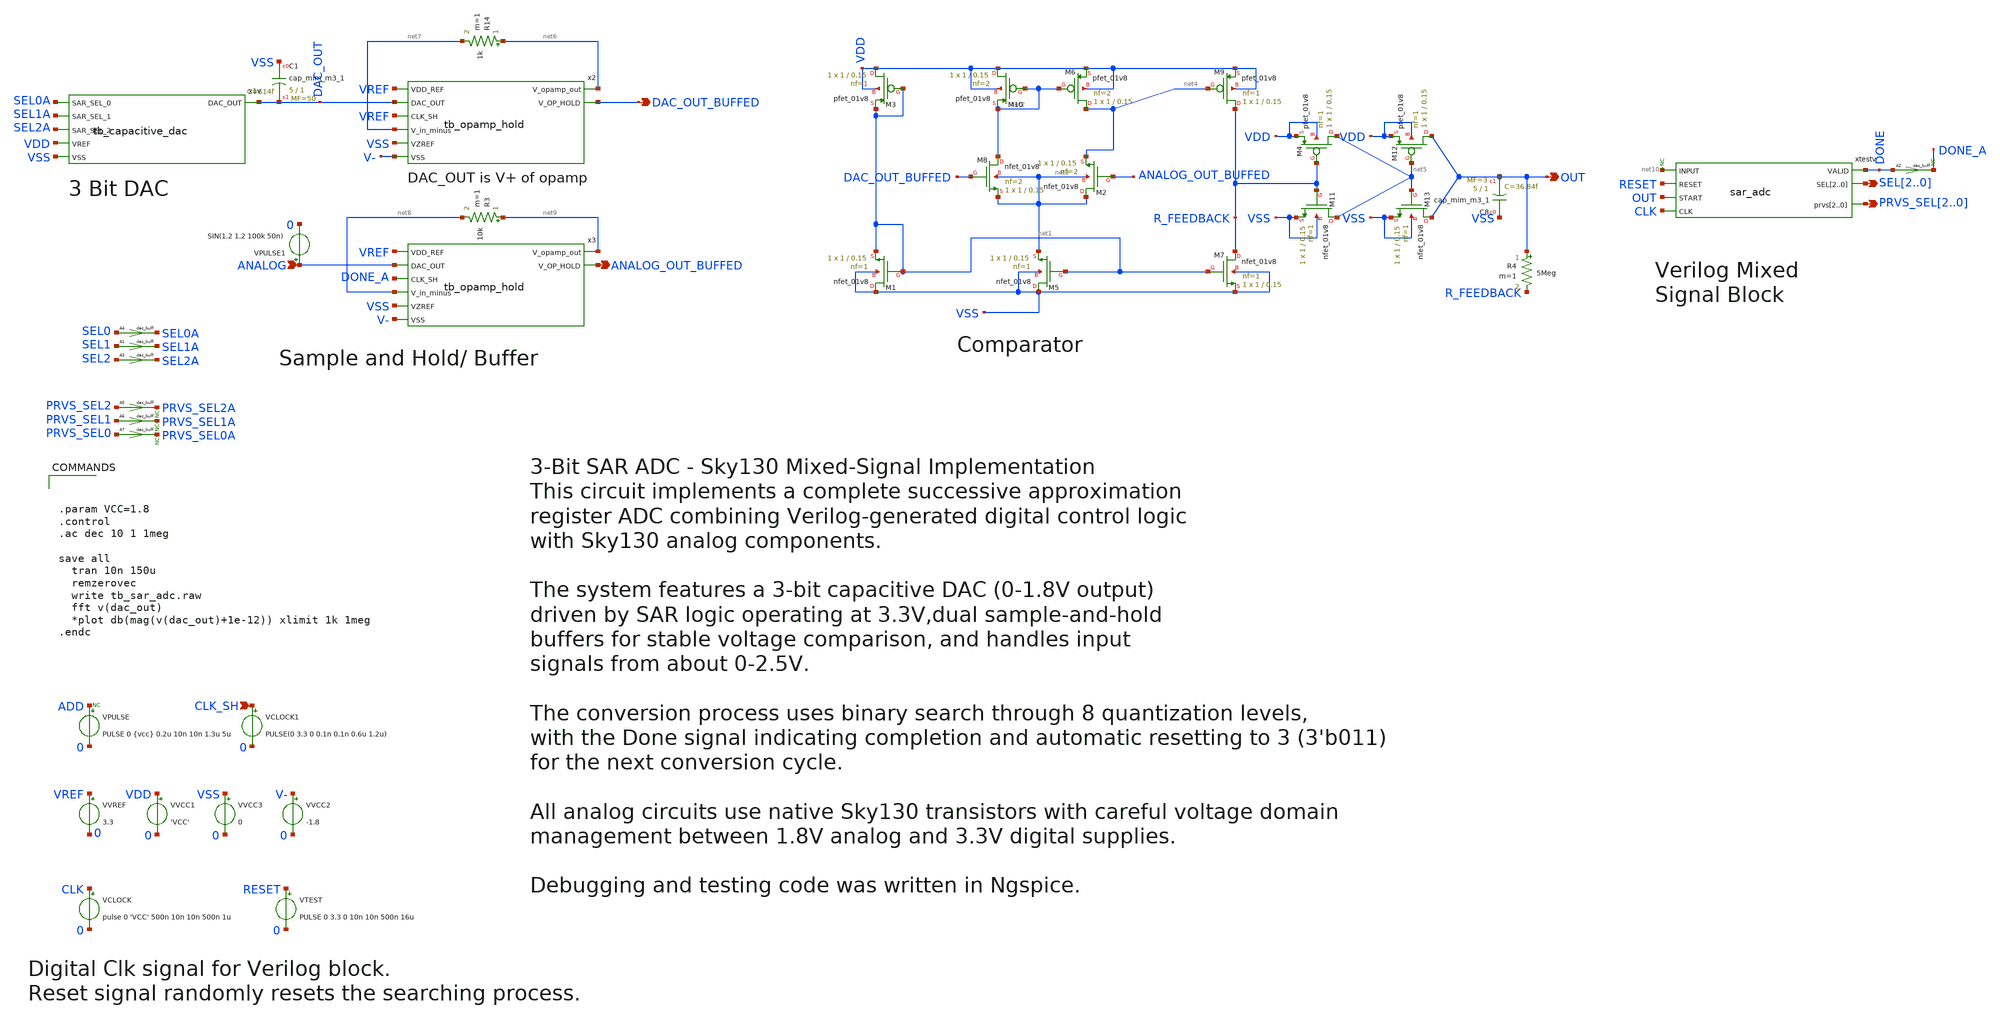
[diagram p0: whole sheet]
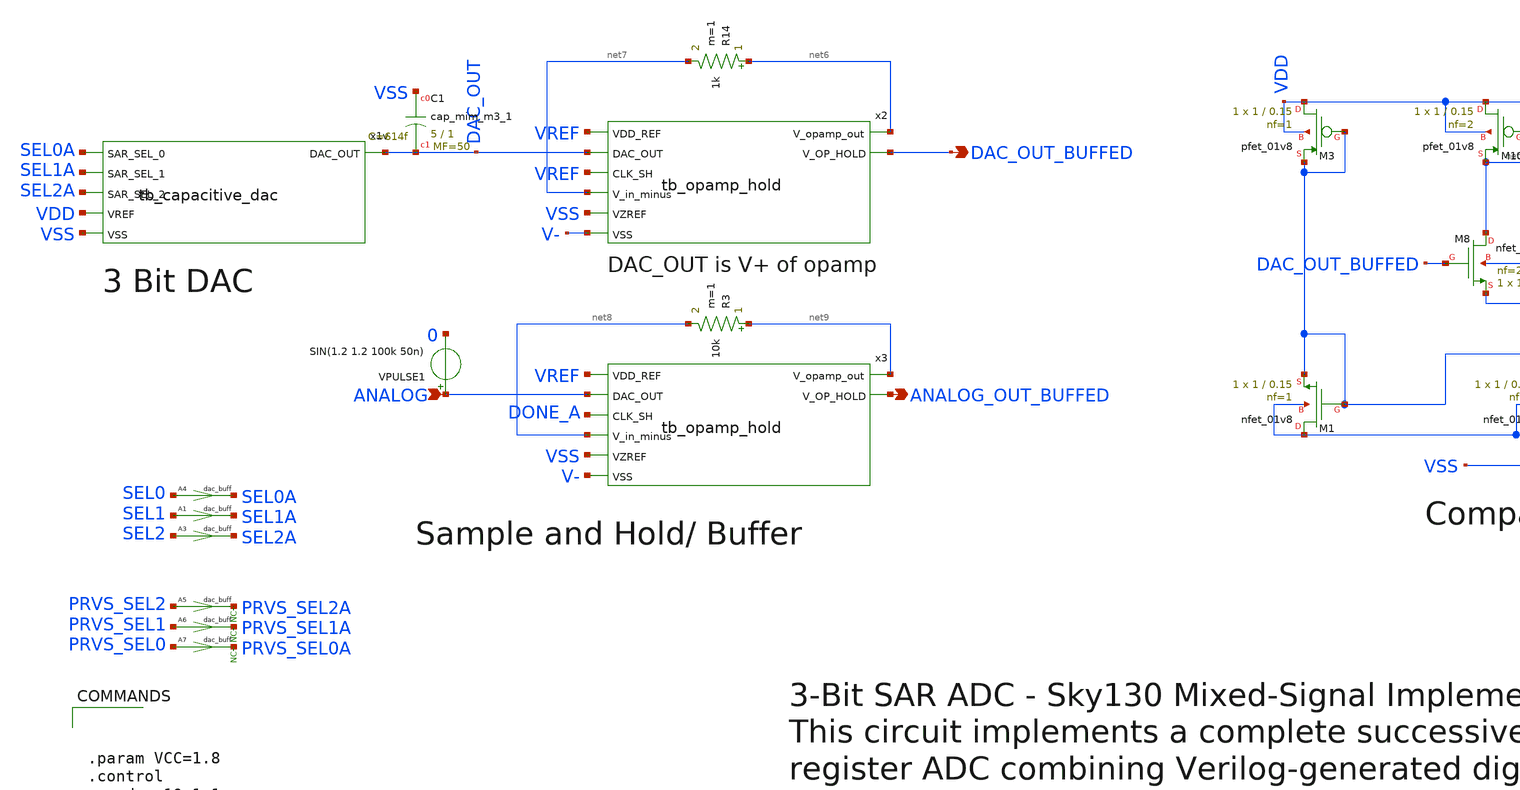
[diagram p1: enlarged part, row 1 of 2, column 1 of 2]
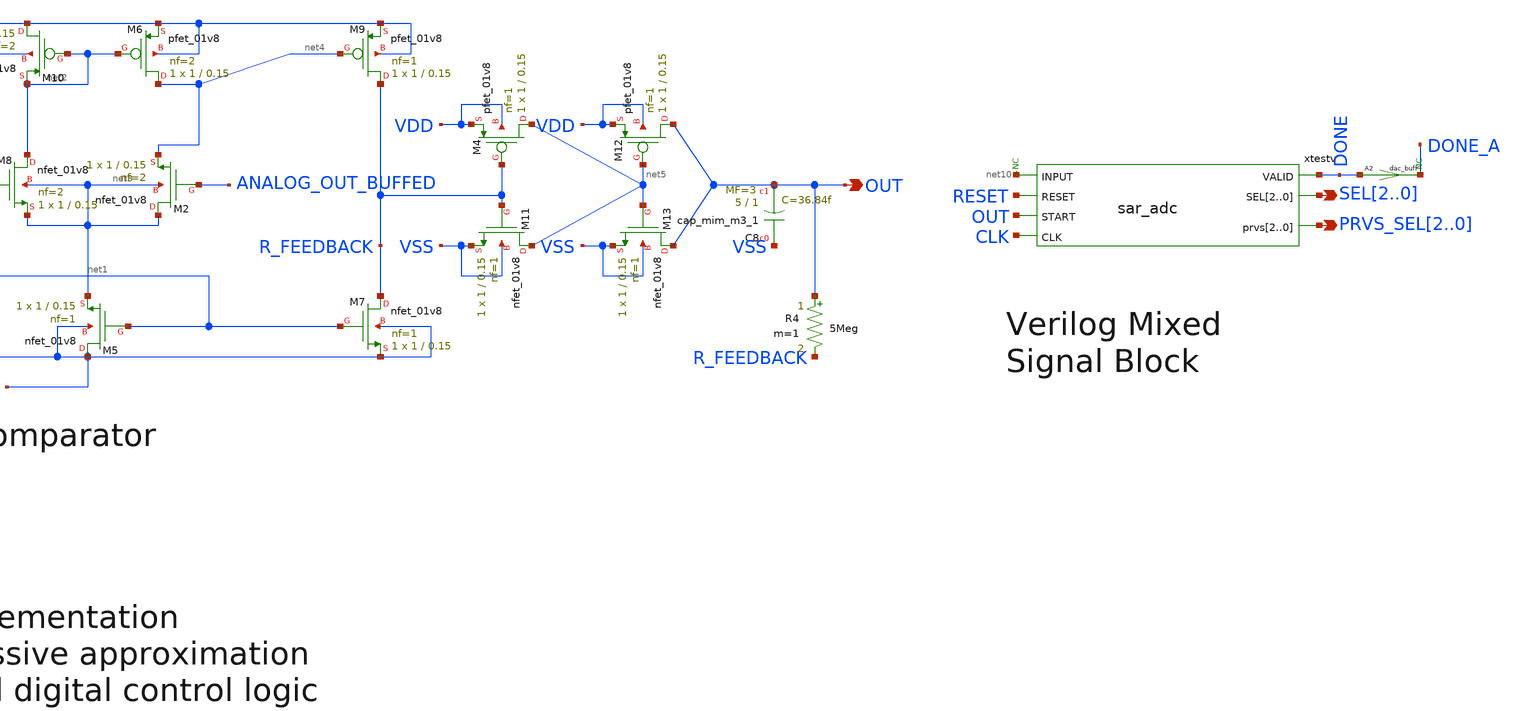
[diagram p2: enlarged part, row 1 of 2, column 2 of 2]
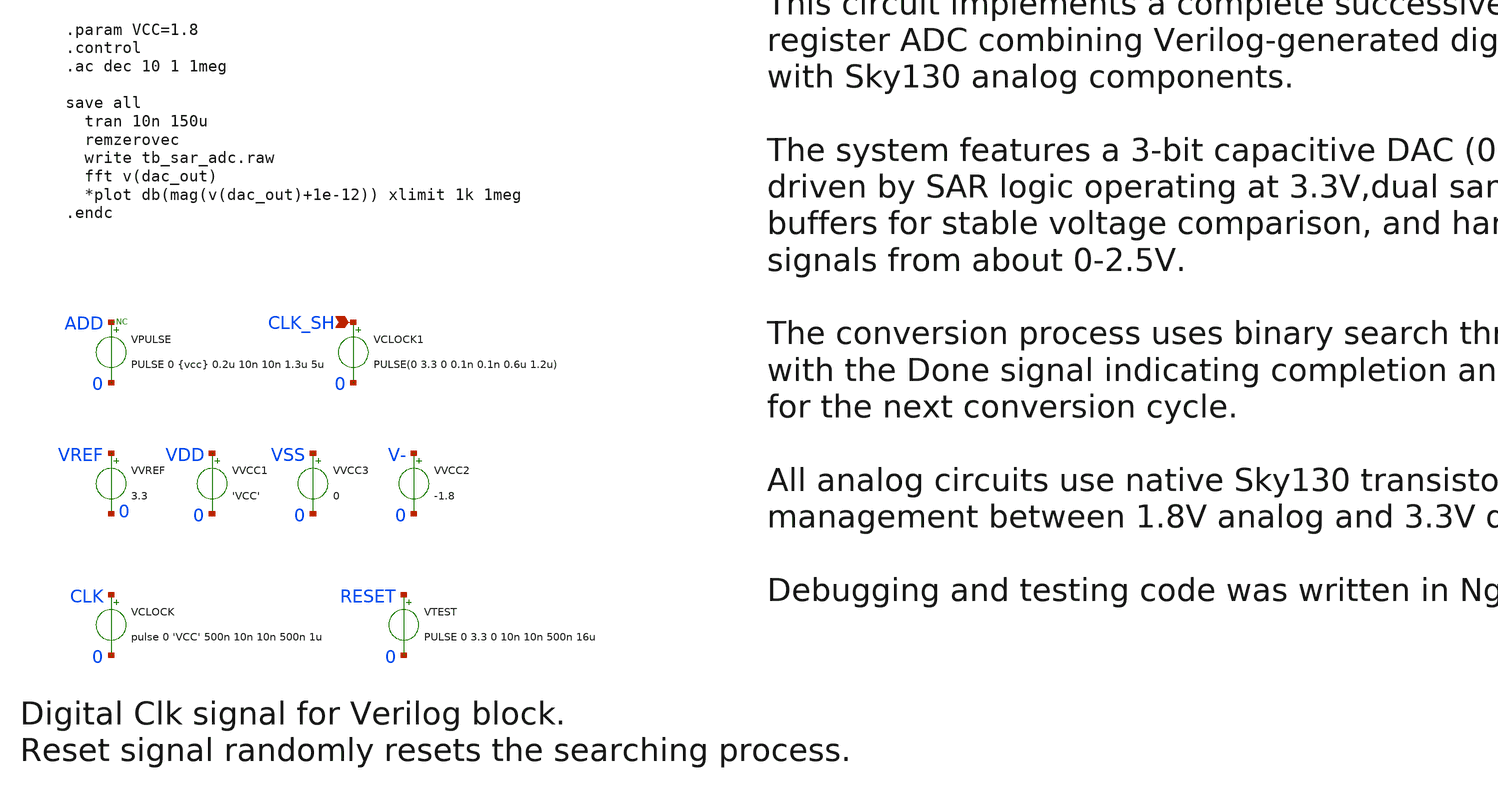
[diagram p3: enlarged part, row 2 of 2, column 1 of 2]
** sch_path: 3bit_sar_adc/tb_sar_adc.sch
**.subckt tb_sar_adc SEL2,SEL1,SEL0 PRVS_SEL2,PRVS_SEL1,PRVS_SEL0 OUT ANALOG DAC_OUT_BUFFED
*+ ANALOG_OUT_BUFFED CLK_SH
*.opin SEL2,SEL1,SEL0
*.opin PRVS_SEL2,PRVS_SEL1,PRVS_SEL0
*.opin OUT
*.ipin ANALOG
*.opin DAC_OUT_BUFFED
*.opin ANALOG_OUT_BUFFED
*.ipin CLK_SH
VPULSE ADD 0 PULSE 0 {vcc} 0.2u 10n 10n 1.3u 5u
VTEST RESET 0 PULSE 0 3.3 0 10n 10n 500n 16u
xtestv net10 RESET OUT DONE SEL2 SEL1 SEL0 CLK PRVS_SEL2 PRVS_SEL1 PRVS_SEL0 sar_adc
A2 [ DONE ] [ DONE_A ] dac_buff
VCLOCK CLK 0 pulse 0 'VCC' 500n 10n 10n 500n 1u
A1 [ SEL1 ] [ SEL1A ] dac_buff
A3 [ SEL2 ] [ SEL2A ] dac_buff
A4 [ SEL0 ] [ SEL0A ] dac_buff
A5 [ PRVS_SEL2 ] [ PRVS_SEL2A ] dac_buff
A6 [ PRVS_SEL1 ] [ PRVS_SEL1A ] dac_buff
A7 [ PRVS_SEL0 ] [ PRVS_SEL0A ] dac_buff
XM9 R_FEEDBACK net4 VDD VDD sky130_fd_pr__pfet_01v8 L=0.15 W=1 nf=1 ad='int((nf+1)/2) * W/nf * 0.29'
+ as='int((nf+2)/2) * W/nf * 0.29' pd='2*int((nf+1)/2) * (W/nf + 0.29)' ps='2*int((nf+2)/2) * (W/nf + 0.29)'
+ nrd='0.29 / W' nrs='0.29 / W' sa=0 sb=0 sd=0 mult=1 m=1
XM6 net4 net2 VDD VDD sky130_fd_pr__pfet_01v8 L=0.15 W=1 nf=2 ad='int((nf+1)/2) * W/nf * 0.29' as='int((nf+2)/2) * W/nf * 0.29'
+ pd='2*int((nf+1)/2) * (W/nf + 0.29)' ps='2*int((nf+2)/2) * (W/nf + 0.29)' nrd='0.29 / W' nrs='0.29 / W'
+ sa=0 sb=0 sd=0 mult=1 m=1
XM10 VDD net2 net2 VDD sky130_fd_pr__pfet_01v8 L=0.15 W=1 nf=2 ad='int((nf+1)/2) * W/nf * 0.29' as='int((nf+2)/2) * W/nf * 0.29'
+ pd='2*int((nf+1)/2) * (W/nf + 0.29)' ps='2*int((nf+2)/2) * (W/nf + 0.29)' nrd='0.29 / W' nrs='0.29 / W'
+ sa=0 sb=0 sd=0 mult=1 m=1
XM3 VDD net1 net1 VDD sky130_fd_pr__pfet_01v8 L=0.15 W=1 nf=1 ad='int((nf+1)/2) * W/nf * 0.29' as='int((nf+2)/2) * W/nf * 0.29'
+ pd='2*int((nf+1)/2) * (W/nf + 0.29)' ps='2*int((nf+2)/2) * (W/nf + 0.29)' nrd='0.29 / W' nrs='0.29 / W'
+ sa=0 sb=0 sd=0 mult=1 m=1
XM4 net5 R_FEEDBACK VDD VDD sky130_fd_pr__pfet_01v8 L=0.15 W=1 nf=1 ad='int((nf+1)/2) * W/nf * 0.29'
+ as='int((nf+2)/2) * W/nf * 0.29' pd='2*int((nf+1)/2) * (W/nf + 0.29)' ps='2*int((nf+2)/2) * (W/nf + 0.29)'
+ nrd='0.29 / W' nrs='0.29 / W' sa=0 sb=0 sd=0 mult=1 m=1
XM12 OUT net5 VDD VDD sky130_fd_pr__pfet_01v8 L=0.15 W=1 nf=1 ad='int((nf+1)/2) * W/nf * 0.29' as='int((nf+2)/2) * W/nf * 0.29'
+ pd='2*int((nf+1)/2) * (W/nf + 0.29)' ps='2*int((nf+2)/2) * (W/nf + 0.29)' nrd='0.29 / W' nrs='0.29 / W'
+ sa=0 sb=0 sd=0 mult=1 m=1
XM2 net3 ANALOG_OUT_BUFFED net4 net3 sky130_fd_pr__nfet_01v8 L=0.15 W=1 nf=2 ad='int((nf+1)/2) * W/nf * 0.29'
+ as='int((nf+2)/2) * W/nf * 0.29' pd='2*int((nf+1)/2) * (W/nf + 0.29)' ps='2*int((nf+2)/2) * (W/nf + 0.29)'
+ nrd='0.29 / W' nrs='0.29 / W' sa=0 sb=0 sd=0 mult=1 m=1
XM1 VSS net1 net1 VSS sky130_fd_pr__nfet_01v8 L=0.15 W=1 nf=1 ad='int((nf+1)/2) * W/nf * 0.29' as='int((nf+2)/2) * W/nf * 0.29'
+ pd='2*int((nf+1)/2) * (W/nf + 0.29)' ps='2*int((nf+2)/2) * (W/nf + 0.29)' nrd='0.29 / W' nrs='0.29 / W'
+ sa=0 sb=0 sd=0 mult=1 m=1
XM5 VSS net1 net3 VSS sky130_fd_pr__nfet_01v8 L=0.15 W=1 nf=1 ad='int((nf+1)/2) * W/nf * 0.29' as='int((nf+2)/2) * W/nf * 0.29'
+ pd='2*int((nf+1)/2) * (W/nf + 0.29)' ps='2*int((nf+2)/2) * (W/nf + 0.29)' nrd='0.29 / W' nrs='0.29 / W'
+ sa=0 sb=0 sd=0 mult=1 m=1
XM7 R_FEEDBACK net1 VSS VSS sky130_fd_pr__nfet_01v8 L=0.15 W=1 nf=1 ad='int((nf+1)/2) * W/nf * 0.29'
+ as='int((nf+2)/2) * W/nf * 0.29' pd='2*int((nf+1)/2) * (W/nf + 0.29)' ps='2*int((nf+2)/2) * (W/nf + 0.29)'
+ nrd='0.29 / W' nrs='0.29 / W' sa=0 sb=0 sd=0 mult=1 m=1
XM8 net2 DAC_OUT_BUFFED net3 net3 sky130_fd_pr__nfet_01v8 L=0.15 W=1 nf=2 ad='int((nf+1)/2) * W/nf * 0.29'
+ as='int((nf+2)/2) * W/nf * 0.29' pd='2*int((nf+1)/2) * (W/nf + 0.29)' ps='2*int((nf+2)/2) * (W/nf + 0.29)'
+ nrd='0.29 / W' nrs='0.29 / W' sa=0 sb=0 sd=0 mult=1 m=1
XM11 net5 R_FEEDBACK VSS VSS sky130_fd_pr__nfet_01v8 L=0.15 W=1 nf=1 ad='int((nf+1)/2) * W/nf * 0.29'
+ as='int((nf+2)/2) * W/nf * 0.29' pd='2*int((nf+1)/2) * (W/nf + 0.29)' ps='2*int((nf+2)/2) * (W/nf + 0.29)'
+ nrd='0.29 / W' nrs='0.29 / W' sa=0 sb=0 sd=0 mult=1 m=1
XM13 OUT net5 VSS VSS sky130_fd_pr__nfet_01v8 L=0.15 W=1 nf=1 ad='int((nf+1)/2) * W/nf * 0.29' as='int((nf+2)/2) * W/nf * 0.29'
+ pd='2*int((nf+1)/2) * (W/nf + 0.29)' ps='2*int((nf+2)/2) * (W/nf + 0.29)' nrd='0.29 / W' nrs='0.29 / W'
+ sa=0 sb=0 sd=0 mult=1 m=1
XC8 VSS OUT sky130_fd_pr__cap_mim_m3_1 W=5 L=1 MF=3 m=3
VVCC1 VDD 0 'VCC'
VPULSE1 ANALOG 0 SIN(1.2 1.2 100k 50n)
x1v DAC_OUT SEL0A SEL1A SEL2A VDD VSS tb_capacitive_dac
x2 VREF DAC_OUT VREF net7 net6 DAC_OUT_BUFFED VSS V- tb_opamp_hold
VVREF VREF 0 3.3
x3 VREF ANALOG DONE_A net8 net9 ANALOG_OUT_BUFFED VSS V- tb_opamp_hold
VVCC3 VSS 0 0
VVCC2 V- 0 -1.8
* noconn DONE_A
* noconn ADD
* noconn PRVS_SEL2A
* noconn PRVS_SEL1A
* noconn PRVS_SEL0A
VCLOCK1 CLK_SH 0 PULSE(0 3.3 0 0.1n 0.1n 0.6u 1.2u)
* noconn #net10
XC1 VSS DAC_OUT sky130_fd_pr__cap_mim_m3_1 W=5 L=1 MF=50 m=50
R14 net6 net7 1k m=1
R3 net9 net8 10k m=1
R4 OUT R_FEEDBACK 5Meg m=1
**** begin user architecture code



.param VCC=1.8
.control
.ac dec 10 1 1meg

save all
  tran 10n 150u
  remzerovec
  write tb_sar_adc.raw
  fft v(dac_out)
  *plot db(mag(v(dac_out)+1e-12)) xlimit 1k 1meg
.endc



** opencircuitdesign pdks install
.lib $::SKYWATER_MODELS/sky130.lib.spice tt
.include $::SKYWATER_STDCELLS/sky130_fd_sc_hd.spice
.include /foss/pdks/sky130A/libs.tech/xschem/sky130_stdcells/

**** end user architecture code
**.ends

* expanding   symbol:  /headless/Documents/3bit_sar_adc/sar_adc.sym # of pins=7
** sym_path: 3bit_sar_adc/sar_adc.sym
** sch_path: 3bit_sar_adc/sar_adc.sch
.subckt sar_adc INPUT RESET START VALID SEL2 SEL1 SEL0 CLK prvs2 prvs1 prvs0
*.ipin INPUT
*.ipin RESET
*.ipin START
*.opin VALID
*.ipin CLK
*.opin SEL2,SEL1,SEL0
*.opin prvs2,prvs1,prvs0
ACOMP [ net2 ] [ net1 ] comparator
ADUT [ CLK RESET START ] [ VALID SEL2 SEL1 SEL0 prvs2 prvs1 prvs0 ] dut
A1 [ COMP ] [ COMP_A ] dac_buff
* noconn #net1
* noconn #net2
* noconn COMP_A
* noconn COMP
* noconn INPUT
.ends


* expanding   symbol:  /headless/Documents/3bit_sar_adc/tb_capacitive_dac.sym # of pins=6
** sym_path: 3bit_sar_adc/tb_capacitive_dac.sym
** sch_path: 3bit_sar_adc/tb_capacitive_dac.sch
.subckt tb_capacitive_dac DAC_OUT SAR_SEL_0 SAR_SEL_1 SAR_SEL_2 VREF VSS
*.opin DAC_OUT
*.ipin SAR_SEL_1
*.ipin SAR_SEL_0
*.ipin SAR_SEL_2
*.ipin VREF
*.ipin VSS
XM20 VSS SAR_SEL_2 S2 S2 sky130_fd_pr__pfet_01v8 L=0.15 W=100 nf=4 ad='int((nf+1)/2) * W/nf * 0.29' as='int((nf+2)/2) * W/nf * 0.29'
+ pd='2*int((nf+1)/2) * (W/nf + 0.29)' ps='2*int((nf+2)/2) * (W/nf + 0.29)' nrd='0.29 / W' nrs='0.29 / W'
+ sa=0 sb=0 sd=0 mult=1 m=1
XM21 VREF SAR_SEL_2 S2 S2 sky130_fd_pr__nfet_01v8 L=0.15 W=150 nf=4 ad='int((nf+1)/2) * W/nf * 0.29'
+ as='int((nf+2)/2) * W/nf * 0.29' pd='2*int((nf+1)/2) * (W/nf + 0.29)' ps='2*int((nf+2)/2) * (W/nf + 0.29)'
+ nrd='0.29 / W' nrs='0.29 / W' sa=0 sb=0 sd=0 mult=1 m=1
XC16 net1 S1 sky130_fd_pr__cap_mim_m3_1 W=5 L=1 MF=400 m=400
XC18 net1 S0 sky130_fd_pr__cap_mim_m3_1 W=5 L=1 MF=200 m=200
XM22 VSS SAR_SEL_1 S1 S1 sky130_fd_pr__pfet_01v8 L=0.15 W=100 nf=10 ad='int((nf+1)/2) * W/nf * 0.29'
+ as='int((nf+2)/2) * W/nf * 0.29' pd='2*int((nf+1)/2) * (W/nf + 0.29)' ps='2*int((nf+2)/2) * (W/nf + 0.29)'
+ nrd='0.29 / W' nrs='0.29 / W' sa=0 sb=0 sd=0 mult=1 m=1
XM23 VREF SAR_SEL_1 S1 S1 sky130_fd_pr__nfet_01v8 L=0.15 W=150 nf=4 ad='int((nf+1)/2) * W/nf * 0.29'
+ as='int((nf+2)/2) * W/nf * 0.29' pd='2*int((nf+1)/2) * (W/nf + 0.29)' ps='2*int((nf+2)/2) * (W/nf + 0.29)'
+ nrd='0.29 / W' nrs='0.29 / W' sa=0 sb=0 sd=0 mult=1 m=1
XM24 VSS SAR_SEL_0 S0 S0 sky130_fd_pr__pfet_01v8 L=0.15 W=100 nf=4 ad='int((nf+1)/2) * W/nf * 0.29' as='int((nf+2)/2) * W/nf * 0.29'
+ pd='2*int((nf+1)/2) * (W/nf + 0.29)' ps='2*int((nf+2)/2) * (W/nf + 0.29)' nrd='0.29 / W' nrs='0.29 / W'
+ sa=0 sb=0 sd=0 mult=1 m=1
XM25 VREF SAR_SEL_0 S0 S0 sky130_fd_pr__nfet_01v8 L=0.15 W=150 nf=4 ad='int((nf+1)/2) * W/nf * 0.29'
+ as='int((nf+2)/2) * W/nf * 0.29' pd='2*int((nf+1)/2) * (W/nf + 0.29)' ps='2*int((nf+2)/2) * (W/nf + 0.29)'
+ nrd='0.29 / W' nrs='0.29 / W' sa=0 sb=0 sd=0 mult=1 m=1
XC22 DAC_OUT VSS sky130_fd_pr__cap_mim_m3_1 W=5 L=1 MF=20 m=20
XC2 net1 S2 sky130_fd_pr__cap_mim_m3_1 W=5 L=1 MF=825 m=825
XC6 VSS S2 sky130_fd_pr__cap_mim_m3_1 W=5 L=1 MF=200 m=200
XC5 VSS S1 sky130_fd_pr__cap_mim_m3_1 W=5 L=1 MF=200 m=200
XC7 VSS S0 sky130_fd_pr__cap_mim_m3_1 W=5 L=1 MF=100 m=100
**** begin user architecture code




.param CAP=80



**** end user architecture code
R1 net1 DAC_OUT 10 m=1
.ends


* expanding   symbol:  /headless/Documents/3bit_sar_adc/tb_opamp_hold.sym # of pins=8
** sym_path: 3bit_sar_adc/tb_opamp_hold.sym
** sch_path: 3bit_sar_adc/tb_opamp_hold.sch
.subckt tb_opamp_hold VDD_REF DAC_OUT CLK_SH V_in_minus V_opamp_out V_OP_HOLD VZREF VSS
*.opin V_opamp_out
*.ipin DAC_OUT
*.ipin CLK_SH
*.opin V_OP_HOLD
*.ipin VDD_REF
*.ipin VZREF
*.ipin VSS
*.ipin V_in_minus
XM82 net1 V_in_minus net3 net3 sky130_fd_pr__pfet_01v8 L=0.6 W=6 nf=1 ad='W * 0.29' as='W * 0.29' pd='2 * (W + 0.29)'
+ ps='2 * (W + 0.29)' nrd='0.29 / W' nrs='0.29 / W' sa=0 sb=0 sd=0 mult=1 m=1
XM84 net2 DAC_OUT net3 net3 sky130_fd_pr__pfet_01v8 L=0.6 W=6 nf=1 ad='W * 0.29' as='W * 0.29' pd='2 * (W + 0.29)'
+ ps='2 * (W + 0.29)' nrd='0.29 / W' nrs='0.29 / W' sa=0 sb=0 sd=0 mult=1 m=1
XM85 net1 net1 VSS VSS sky130_fd_pr__nfet_01v8 L=0.6 W=6 nf=1 ad='W * 0.29' as='W * 0.29' pd='2 * (W + 0.29)'
+ ps='2 * (W + 0.29)' nrd='0.29 / W' nrs='0.29 / W' sa=0 sb=0 sd=0 mult=1 m=1
XM86 net2 net1 VSS VSS sky130_fd_pr__nfet_01v8 L=0.6 W=6 nf=1 ad='W * 0.29' as='W * 0.29' pd='2 * (W + 0.29)'
+ ps='2 * (W + 0.29)' nrd='0.29 / W' nrs='0.29 / W' sa=0 sb=0 sd=0 mult=1 m=1
XM87 net3 VSS VDD_REF VDD_REF sky130_fd_pr__pfet_01v8 L=0.6 W=6 nf=1 ad='W * 0.29' as='W * 0.29' pd='2 * (W + 0.29)'
+ ps='2 * (W + 0.29)' nrd='0.29 / W' nrs='0.29 / W' sa=0 sb=0 sd=0 mult=1 m=1
XM88 V_opamp_out VSS VDD_REF VDD_REF sky130_fd_pr__pfet_01v8 L=0.6 W=6 nf=1 ad='W * 0.29' as='W * 0.29'
+ pd='2 * (W + 0.29)' ps='2 * (W + 0.29)' nrd='0.29 / W' nrs='0.29 / W' sa=0 sb=0 sd=0 mult=1 m=1
XM89 VZREF VSS VDD_REF VDD_REF sky130_fd_pr__pfet_01v8 L=0.6 W=6 nf=1 ad='W * 0.29' as='W * 0.29' pd='2 * (W + 0.29)'
+ ps='2 * (W + 0.29)' nrd='0.29 / W' nrs='0.29 / W' sa=0 sb=0 sd=0 mult=1 m=1
XM90 net4 VDD_REF net2 VSS sky130_fd_pr__nfet_01v8 L=0.6 W=1 nf=1 ad='W * 0.29' as='W * 0.29' pd='2 * (W + 0.29)'
+ ps='2 * (W + 0.29)' nrd='0.29 / W' nrs='0.29 / W' sa=0 sb=0 sd=0 mult=1 m=1
XM91 V_opamp_out net2 VSS VSS sky130_fd_pr__nfet_01v8 L=0.6 W=6 nf=1 ad='W * 0.29' as='W * 0.29' pd='2 * (W + 0.29)'
+ ps='2 * (W + 0.29)' nrd='0.29 / W' nrs='0.29 / W' sa=0 sb=0 sd=0 mult=1 m=1
XR10 VSS VZREF VSS sky130_fd_pr__res_high_po W=1 L=1 mult=1 m=1
XR13 VZREF VDD_REF VSS sky130_fd_pr__res_high_po W=1 L=1 mult=1 m=1
C34 V_opamp_out net4 0.8p m=1
XM80 V_OP_HOLD CLK_SH V_opamp_out VZREF sky130_fd_pr__nfet_01v8 L=0.6 W=6 nf=1 ad='W * 0.29' as='W * 0.29'
+ pd='2 * (W + 0.29)' ps='2 * (W + 0.29)' nrd='0.29 / W' nrs='0.29 / W' sa=0 sb=0 sd=0 mult=1 m=1
XC1 V_OP_HOLD VZREF sky130_fd_pr__cap_mim_m3_1 W=5 L=1 MF=42 m=42
.ends

**** begin user architecture code
.model dut d_cosim simulation="./three_bit_adc.so"
.model comparator adc_bridge in_low=0 in_high=3.3
.model dac_buff dac_bridge input_load=1e-15 t_rise=10n t_fall=10n  out_low=0 out_high=3.3
**** end user architecture code
.end
